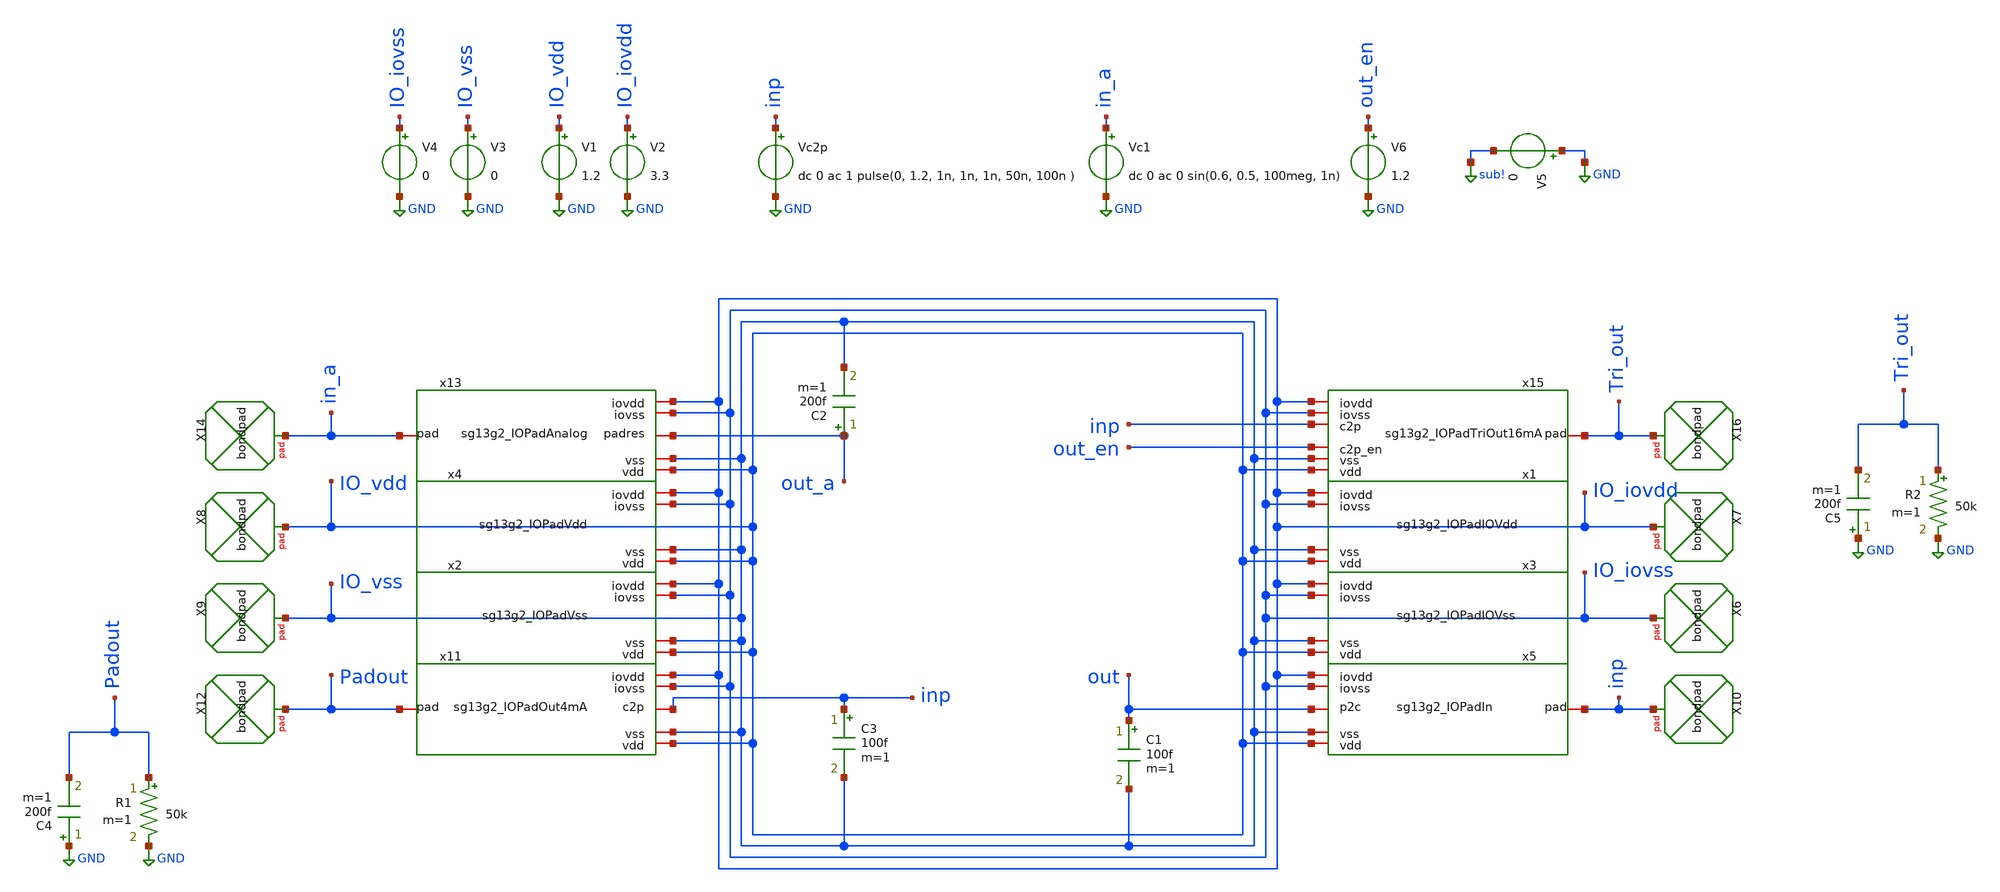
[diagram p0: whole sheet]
** sch_path: ihp-sg13g2/libs.tech/xschem/sg13g2_io_tests/Power_IO.sch
**.subckt Power_IO
V1 IO_vdd GND 1.2
V2 IO_iovdd GND 3.3
V3 IO_vss GND 0
V4 IO_iovss GND 0
Vc2p inp GND dc 0 ac 1 pulse(0, 1.2, 1n, 1n, 1n, 50n, 100n )
x1 IO_iovdd IO_iovss IO_vss IO_vdd sg13g2_IOPadIOVdd
x3 IO_iovdd IO_iovss IO_vss IO_vdd sg13g2_IOPadIOVss
x2 IO_iovdd IO_iovss IO_vss IO_vdd sg13g2_IOPadVSS
x4 IO_iovdd IO_iovss IO_vss IO_vdd sg13g2_IOPadVdd
x5 IO_iovdd IO_iovss out IO_vss IO_vdd inp sg13g2_IOPadIn
C1 out IO_vss 100f m=1
XX6 IO_iovss bondpad size=80u shape=0 padtype=0
XX7 IO_iovdd bondpad size=80u shape=0 padtype=0
XX8 IO_vdd bondpad size=80u shape=0 padtype=0
XX9 IO_vss bondpad size=80u shape=0 padtype=0
XX10 inp bondpad size=80u shape=0 padtype=0
XX12 Padout bondpad size=80u shape=0 padtype=0
x13 IO_iovdd IO_iovss out_a IO_vss IO_vdd in_a sg13g2_IOPadAnalog
C2 out_a IO_vss 200f m=1
XX14 in_a bondpad size=80u shape=0 padtype=0
Vc1 in_a GND dc 0 ac 0 sin(0.6, 0.5, 100meg, 1n)
V5 GND sub! 0
C3 inp IO_vss 100f m=1
V6 out_en GND 1.2
x11 IO_iovdd IO_iovss inp IO_vss IO_vdd Padout sg13g2_IOPadOut4mA
x15 IO_iovdd IO_iovss inp out_en IO_vss IO_vdd Tri_out sg13g2_IOPadTriOut16mA
XX16 Tri_out bondpad size=80u shape=0 padtype=0
C5 GND Tri_out 200f m=1
R2 Tri_out GND 50k m=1
C4 GND Padout 200f m=1
R1 Padout GND 50k m=1
**** begin user architecture code

.lib cornerMOSlv.lib mos_tt
.lib cornerMOShv.lib mos_tt
.lib cornerRES.lib res_typ
.include diodes.lib
.include sg13g2_bondpad.lib



.param temp=27
*.OPTION RSHUNT=1e6
.OPTION CSHUNT=1e-13
.option rseries = 10.0e-0
.options method=gear reltol=1e-3 abstol=1e-6
*.options gmin=1e-10
*.ic V(out)=0

.control
save all
tran  601p 180n
meas tran tdelayf TRIG v(inp) VAl=0.6 FALl=1 TARG v(out) VAl=0.6 FALL=1
meas tran tdelayr TRIG v(inp) VAl=0.6 RISE=2 TARG v(out) VAl=0.6 RISE=2
write power_io.raw


.endc


**** end user architecture code
**.ends
.GLOBAL GND
.GLOBAL sub!
.end
